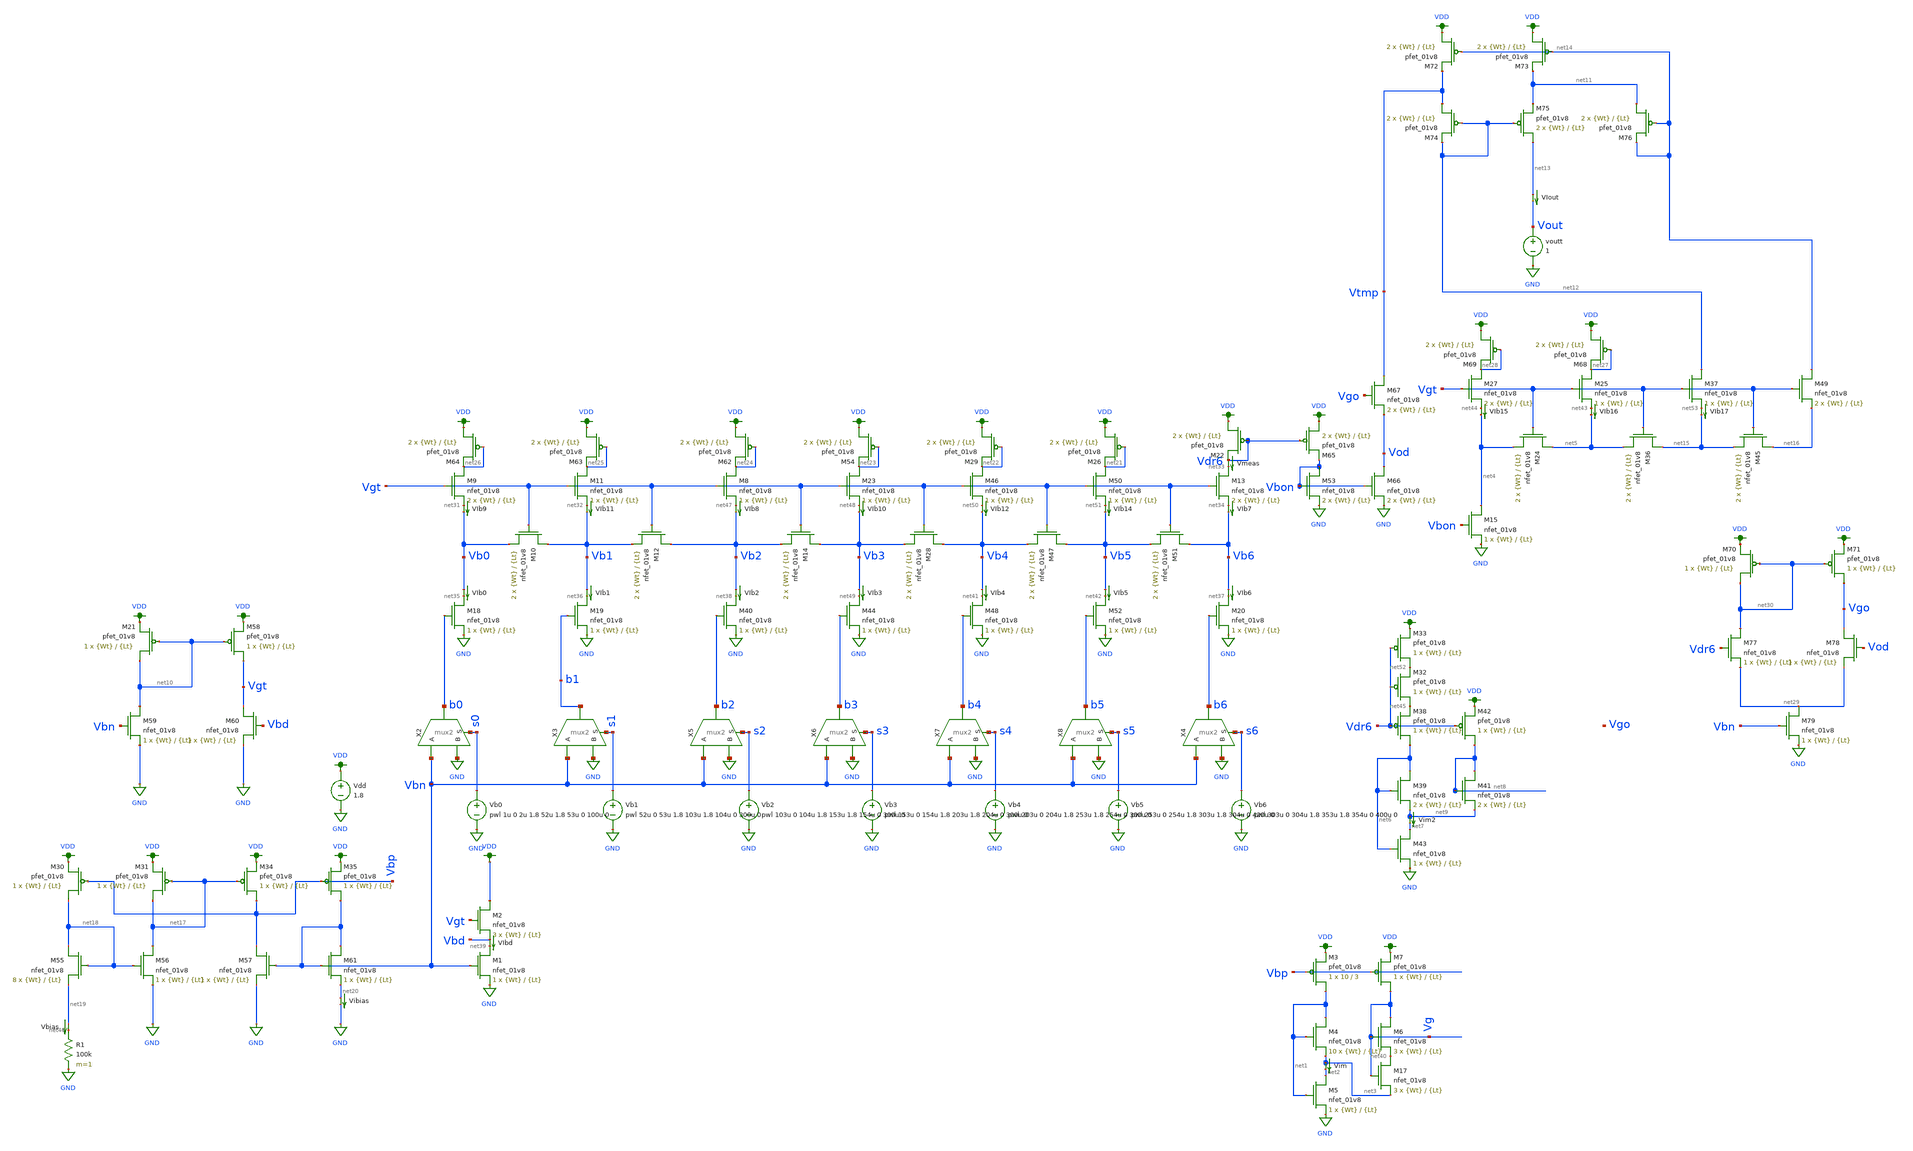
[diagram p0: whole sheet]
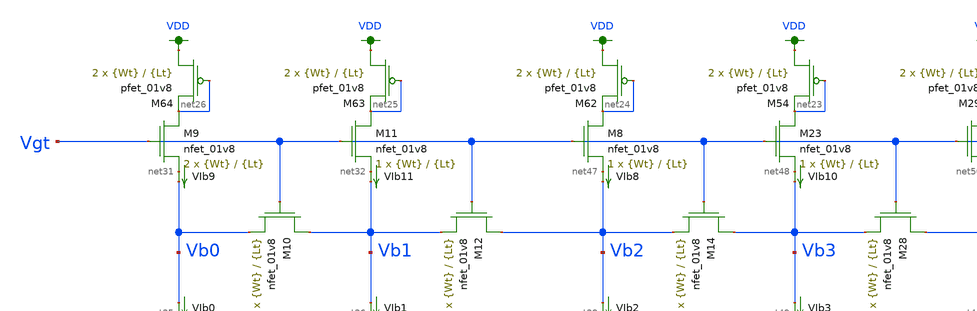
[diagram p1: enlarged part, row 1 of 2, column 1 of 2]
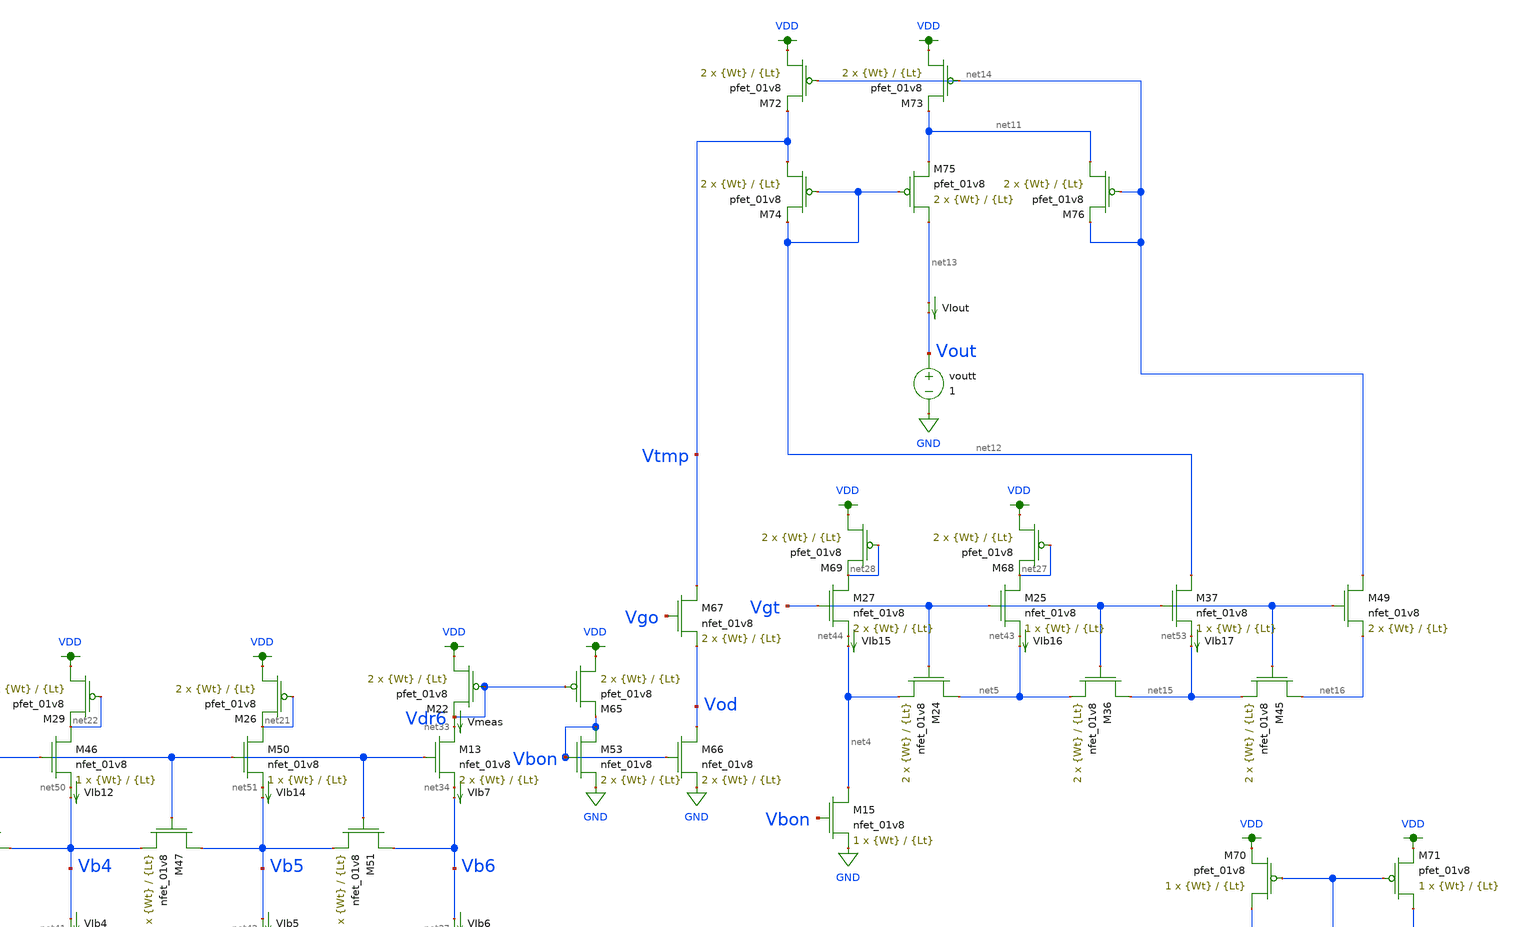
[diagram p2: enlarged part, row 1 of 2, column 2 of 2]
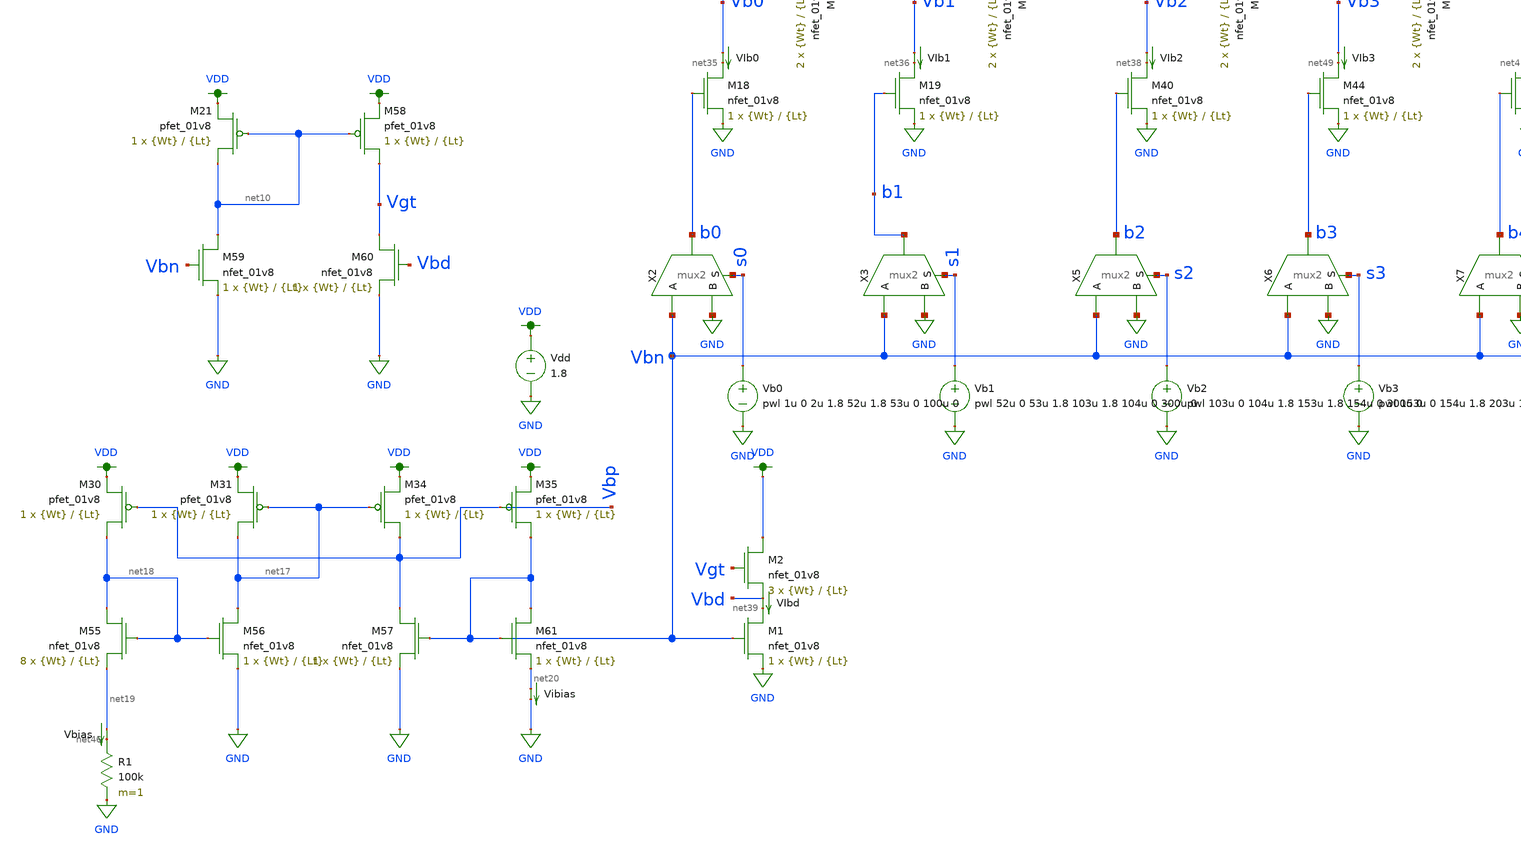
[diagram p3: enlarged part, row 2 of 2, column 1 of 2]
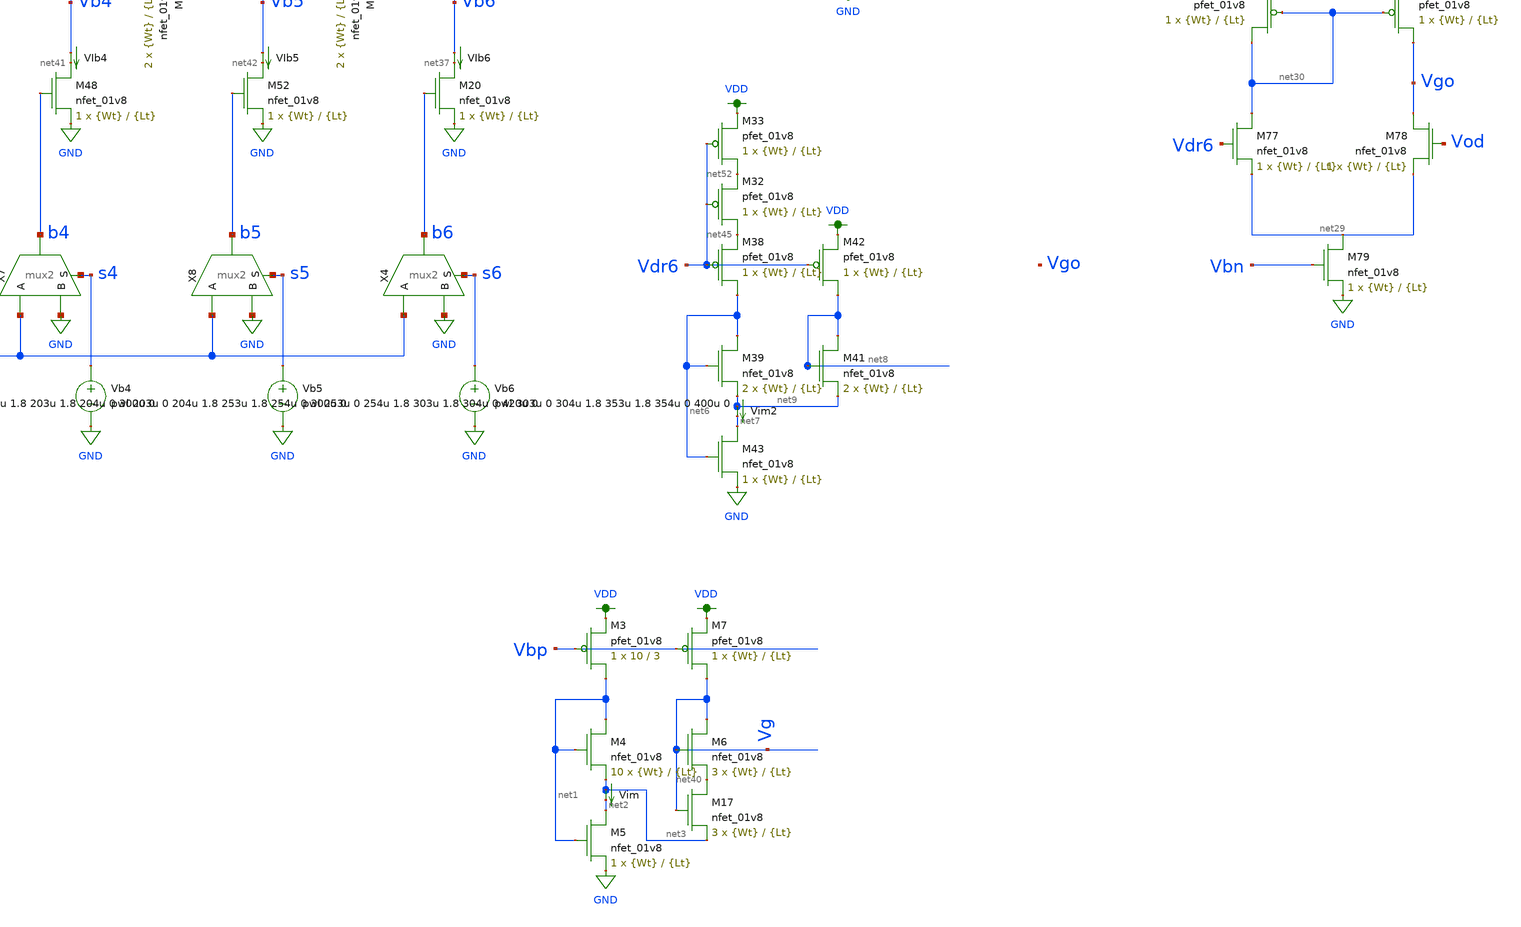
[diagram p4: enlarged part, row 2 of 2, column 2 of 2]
** sch_path: schematic/archive/dac7_test_josh_mywilson_idnl.sch
**.subckt dac7_test_josh_mywilson_idnl
X2 b0 Vbn GND s0 mux2
X3 b1 Vbn GND s1 mux2
Vdd VDD GND 1.8
Vb0 s0 GND pwl 1u 0 2u 1.8 52u 1.8 53u 0 100u 0
Vb1 s1 GND pwl 52u 0 53u 1.8 103u 1.8 104u 0 300u 0
Vb2 s2 GND pwl 103u 0 104u 1.8 153u 1.8 154u 0 300u 0
XM9 net26 Vgt net31 GND sky130_fd_pr__nfet_01v8 L={Lt} W={Wt} nf=1 ad='int((nf+1)/2) * W/nf * 0.29' as='int((nf+2)/2) * W/nf * 0.29'
+ pd='2*int((nf+1)/2) * (W/nf + 0.29)' ps='2*int((nf+2)/2) * (W/nf + 0.29)' nrd='0.29 / W' nrs='0.29 / W'
+ sa=0 sb=0 sd=0 mult=2 m=2
XM10 Vb1 Vgt Vb0 GND sky130_fd_pr__nfet_01v8 L={Lt} W={Wt} nf=1 ad='int((nf+1)/2) * W/nf * 0.29' as='int((nf+2)/2) * W/nf * 0.29'
+ pd='2*int((nf+1)/2) * (W/nf + 0.29)' ps='2*int((nf+2)/2) * (W/nf + 0.29)' nrd='0.29 / W' nrs='0.29 / W'
+ sa=0 sb=0 sd=0 mult=2 m=2
XM11 net25 Vgt net32 GND sky130_fd_pr__nfet_01v8 L={Lt} W={Wt} nf=1 ad='int((nf+1)/2) * W/nf * 0.29'
+ as='int((nf+2)/2) * W/nf * 0.29' pd='2*int((nf+1)/2) * (W/nf + 0.29)' ps='2*int((nf+2)/2) * (W/nf + 0.29)'
+ nrd='0.29 / W' nrs='0.29 / W' sa=0 sb=0 sd=0 mult=1 m=1
XM12 Vb2 Vgt Vb1 GND sky130_fd_pr__nfet_01v8 L={Lt} W={Wt} nf=1 ad='int((nf+1)/2) * W/nf * 0.29' as='int((nf+2)/2) * W/nf * 0.29'
+ pd='2*int((nf+1)/2) * (W/nf + 0.29)' ps='2*int((nf+2)/2) * (W/nf + 0.29)' nrd='0.29 / W' nrs='0.29 / W'
+ sa=0 sb=0 sd=0 mult=2 m=2
XM13 net33 Vgt net34 GND sky130_fd_pr__nfet_01v8 L={Lt} W={Wt} nf=1 ad='int((nf+1)/2) * W/nf * 0.29'
+ as='int((nf+2)/2) * W/nf * 0.29' pd='2*int((nf+1)/2) * (W/nf + 0.29)' ps='2*int((nf+2)/2) * (W/nf + 0.29)'
+ nrd='0.29 / W' nrs='0.29 / W' sa=0 sb=0 sd=0 mult=2 m=2
XM18 net35 b0 GND GND sky130_fd_pr__nfet_01v8 L={Lt} W={Wt} nf=1 ad='int((nf+1)/2) * W/nf * 0.29' as='int((nf+2)/2) * W/nf * 0.29'
+ pd='2*int((nf+1)/2) * (W/nf + 0.29)' ps='2*int((nf+2)/2) * (W/nf + 0.29)' nrd='0.29 / W' nrs='0.29 / W'
+ sa=0 sb=0 sd=0 mult=1 m=1
XM19 net36 b1 GND GND sky130_fd_pr__nfet_01v8 L={Lt} W={Wt} nf=1 ad='int((nf+1)/2) * W/nf * 0.29' as='int((nf+2)/2) * W/nf * 0.29'
+ pd='2*int((nf+1)/2) * (W/nf + 0.29)' ps='2*int((nf+2)/2) * (W/nf + 0.29)' nrd='0.29 / W' nrs='0.29 / W'
+ sa=0 sb=0 sd=0 mult=1 m=1
XM20 net37 b6 GND GND sky130_fd_pr__nfet_01v8 L={Lt} W={Wt} nf=1 ad='int((nf+1)/2) * W/nf * 0.29' as='int((nf+2)/2) * W/nf * 0.29'
+ pd='2*int((nf+1)/2) * (W/nf + 0.29)' ps='2*int((nf+2)/2) * (W/nf + 0.29)' nrd='0.29 / W' nrs='0.29 / W'
+ sa=0 sb=0 sd=0 mult=1 m=1
Vmeas Vdr6 net33 0
.save i(vmeas)
VIb0 Vb0 net35 0
.save i(vib0)
VIb1 Vb1 net36 0
.save i(vib1)
VIb2 Vb2 net38 0
.save i(vib2)
XM1 net39 Vbn GND GND sky130_fd_pr__nfet_01v8 L={Lt} W={Wt} nf=1 ad='int((nf+1)/2) * W/nf * 0.29' as='int((nf+2)/2) * W/nf * 0.29'
+ pd='2*int((nf+1)/2) * (W/nf + 0.29)' ps='2*int((nf+2)/2) * (W/nf + 0.29)' nrd='0.29 / W' nrs='0.29 / W'
+ sa=0 sb=0 sd=0 mult=1 m=1
VIbd Vbd net39 0
.save i(vibd)
XM3 net1 Vbp VDD VDD sky130_fd_pr__pfet_01v8 L=3 W=10 nf=1 ad='int((nf+1)/2) * W/nf * 0.29' as='int((nf+2)/2) * W/nf * 0.29'
+ pd='2*int((nf+1)/2) * (W/nf + 0.29)' ps='2*int((nf+2)/2) * (W/nf + 0.29)' nrd='0.29 / W' nrs='0.29 / W'
+ sa=0 sb=0 sd=0 mult=1 m=1
XM4 net1 net1 net3 GND sky130_fd_pr__nfet_01v8 L={Lt} W={Wt} nf=1 ad='int((nf+1)/2) * W/nf * 0.29' as='int((nf+2)/2) * W/nf * 0.29'
+ pd='2*int((nf+1)/2) * (W/nf + 0.29)' ps='2*int((nf+2)/2) * (W/nf + 0.29)' nrd='0.29 / W' nrs='0.29 / W'
+ sa=0 sb=0 sd=0 mult=10 m=10
XM5 net2 net1 GND GND sky130_fd_pr__nfet_01v8 L={Lt} W={Wt} nf=1 ad='int((nf+1)/2) * W/nf * 0.29' as='int((nf+2)/2) * W/nf * 0.29'
+ pd='2*int((nf+1)/2) * (W/nf + 0.29)' ps='2*int((nf+2)/2) * (W/nf + 0.29)' nrd='0.29 / W' nrs='0.29 / W'
+ sa=0 sb=0 sd=0 mult=1 m=1
Vim net3 net2 0
.save i(vim)
XM6 Vg Vg net40 GND sky130_fd_pr__nfet_01v8 L={Lt} W={Wt} nf=1 ad='int((nf+1)/2) * W/nf * 0.29' as='int((nf+2)/2) * W/nf * 0.29'
+ pd='2*int((nf+1)/2) * (W/nf + 0.29)' ps='2*int((nf+2)/2) * (W/nf + 0.29)' nrd='0.29 / W' nrs='0.29 / W'
+ sa=0 sb=0 sd=0 mult=3 m=3
XM7 Vg Vbp VDD VDD sky130_fd_pr__pfet_01v8 L={Lt} W={Wt} nf=1 ad='int((nf+1)/2) * W/nf * 0.29' as='int((nf+2)/2) * W/nf * 0.29'
+ pd='2*int((nf+1)/2) * (W/nf + 0.29)' ps='2*int((nf+2)/2) * (W/nf + 0.29)' nrd='0.29 / W' nrs='0.29 / W'
+ sa=0 sb=0 sd=0 mult=1 m=1
VIb4 Vb4 net41 0
.save i(vib4)
VIb5 Vb5 net42 0
.save i(vib5)
VIb6 Vb6 net37 0
.save i(vib6)
VIout net13 Vout 0
.save i(viout)
XM24 net5 Vgt net4 GND sky130_fd_pr__nfet_01v8 L={Lt} W={Wt} nf=1 ad='int((nf+1)/2) * W/nf * 0.29' as='int((nf+2)/2) * W/nf * 0.29'
+ pd='2*int((nf+1)/2) * (W/nf + 0.29)' ps='2*int((nf+2)/2) * (W/nf + 0.29)' nrd='0.29 / W' nrs='0.29 / W'
+ sa=0 sb=0 sd=0 mult=2 m=2
XM25 net27 Vgt net43 GND sky130_fd_pr__nfet_01v8 L={Lt} W={Wt} nf=1 ad='int((nf+1)/2) * W/nf * 0.29'
+ as='int((nf+2)/2) * W/nf * 0.29' pd='2*int((nf+1)/2) * (W/nf + 0.29)' ps='2*int((nf+2)/2) * (W/nf + 0.29)'
+ nrd='0.29 / W' nrs='0.29 / W' sa=0 sb=0 sd=0 mult=1 m=1
XM27 net28 Vgt net44 GND sky130_fd_pr__nfet_01v8 L={Lt} W={Wt} nf=1 ad='int((nf+1)/2) * W/nf * 0.29'
+ as='int((nf+2)/2) * W/nf * 0.29' pd='2*int((nf+1)/2) * (W/nf + 0.29)' ps='2*int((nf+2)/2) * (W/nf + 0.29)'
+ nrd='0.29 / W' nrs='0.29 / W' sa=0 sb=0 sd=0 mult=2 m=2
XM38 net6 Vdr6 net45 VDD sky130_fd_pr__pfet_01v8 L={Lt} W={Wt} nf=1 ad='int((nf+1)/2) * W/nf * 0.29'
+ as='int((nf+2)/2) * W/nf * 0.29' pd='2*int((nf+1)/2) * (W/nf + 0.29)' ps='2*int((nf+2)/2) * (W/nf + 0.29)'
+ nrd='0.29 / W' nrs='0.29 / W' sa=0 sb=0 sd=0 mult=1 m=1
XM39 net6 net6 net9 GND sky130_fd_pr__nfet_01v8 L={Lt} W={Wt} nf=1 ad='int((nf+1)/2) * W/nf * 0.29' as='int((nf+2)/2) * W/nf * 0.29'
+ pd='2*int((nf+1)/2) * (W/nf + 0.29)' ps='2*int((nf+2)/2) * (W/nf + 0.29)' nrd='0.29 / W' nrs='0.29 / W'
+ sa=0 sb=0 sd=0 mult=2 m=2
Vim2 net9 net7 0
.save i(vim2)
XM41 net8 net8 net9 GND sky130_fd_pr__nfet_01v8 L={Lt} W={Wt} nf=1 ad='int((nf+1)/2) * W/nf * 0.29' as='int((nf+2)/2) * W/nf * 0.29'
+ pd='2*int((nf+1)/2) * (W/nf + 0.29)' ps='2*int((nf+2)/2) * (W/nf + 0.29)' nrd='0.29 / W' nrs='0.29 / W'
+ sa=0 sb=0 sd=0 mult=2 m=2
XM42 net8 Vdr6 VDD VDD sky130_fd_pr__pfet_01v8 L={Lt} W={Wt} nf=1 ad='int((nf+1)/2) * W/nf * 0.29' as='int((nf+2)/2) * W/nf * 0.29'
+ pd='2*int((nf+1)/2) * (W/nf + 0.29)' ps='2*int((nf+2)/2) * (W/nf + 0.29)' nrd='0.29 / W' nrs='0.29 / W'
+ sa=0 sb=0 sd=0 mult=1 m=1
XM43 net7 net6 GND GND sky130_fd_pr__nfet_01v8 L={Lt} W={Wt} nf=1 ad='int((nf+1)/2) * W/nf * 0.29' as='int((nf+2)/2) * W/nf * 0.29'
+ pd='2*int((nf+1)/2) * (W/nf + 0.29)' ps='2*int((nf+2)/2) * (W/nf + 0.29)' nrd='0.29 / W' nrs='0.29 / W'
+ sa=0 sb=0 sd=0 mult=1 m=1
XM2 VDD Vgt Vbd GND sky130_fd_pr__nfet_01v8 L={Lt} W={Wt} nf=1 ad='int((nf+1)/2) * W/nf * 0.29' as='int((nf+2)/2) * W/nf * 0.29'
+ pd='2*int((nf+1)/2) * (W/nf + 0.29)' ps='2*int((nf+2)/2) * (W/nf + 0.29)' nrd='0.29 / W' nrs='0.29 / W'
+ sa=0 sb=0 sd=0 mult=3 m=3
XM17 net40 Vg net3 GND sky130_fd_pr__nfet_01v8 L={Lt} W={Wt} nf=1 ad='int((nf+1)/2) * W/nf * 0.29' as='int((nf+2)/2) * W/nf * 0.29'
+ pd='2*int((nf+1)/2) * (W/nf + 0.29)' ps='2*int((nf+2)/2) * (W/nf + 0.29)' nrd='0.29 / W' nrs='0.29 / W'
+ sa=0 sb=0 sd=0 mult=3 m=3
XM21 net10 net10 VDD VDD sky130_fd_pr__pfet_01v8 L={Lt} W={Wt} nf=1 ad='int((nf+1)/2) * W/nf * 0.29'
+ as='int((nf+2)/2) * W/nf * 0.29' pd='2*int((nf+1)/2) * (W/nf + 0.29)' ps='2*int((nf+2)/2) * (W/nf + 0.29)'
+ nrd='0.29 / W' nrs='0.29 / W' sa=0 sb=0 sd=0 mult=1 m=1
XM58 Vgt net10 VDD VDD sky130_fd_pr__pfet_01v8 L={Lt} W={Wt} nf=1 ad='int((nf+1)/2) * W/nf * 0.29' as='int((nf+2)/2) * W/nf * 0.29'
+ pd='2*int((nf+1)/2) * (W/nf + 0.29)' ps='2*int((nf+2)/2) * (W/nf + 0.29)' nrd='0.29 / W' nrs='0.29 / W'
+ sa=0 sb=0 sd=0 mult=1 m=1
XM59 net10 Vbn GND GND sky130_fd_pr__nfet_01v8 L={Lt} W={Wt} nf=1 ad='int((nf+1)/2) * W/nf * 0.29' as='int((nf+2)/2) * W/nf * 0.29'
+ pd='2*int((nf+1)/2) * (W/nf + 0.29)' ps='2*int((nf+2)/2) * (W/nf + 0.29)' nrd='0.29 / W' nrs='0.29 / W'
+ sa=0 sb=0 sd=0 mult=1 m=1
XM60 Vgt Vbd GND GND sky130_fd_pr__nfet_01v8 L={Lt} W={Wt} nf=1 ad='int((nf+1)/2) * W/nf * 0.29' as='int((nf+2)/2) * W/nf * 0.29'
+ pd='2*int((nf+1)/2) * (W/nf + 0.29)' ps='2*int((nf+2)/2) * (W/nf + 0.29)' nrd='0.29 / W' nrs='0.29 / W'
+ sa=0 sb=0 sd=0 mult=1 m=1
XM72 VDD net14 Vtmp VDD sky130_fd_pr__pfet_01v8 L={Lt} W={Wt} nf=1 ad='int((nf+1)/2) * W/nf * 0.29' as='int((nf+2)/2) * W/nf * 0.29'
+ pd='2*int((nf+1)/2) * (W/nf + 0.29)' ps='2*int((nf+2)/2) * (W/nf + 0.29)' nrd='0.29 / W' nrs='0.29 / W'
+ sa=0 sb=0 sd=0 mult=2 m=2
XM73 VDD net14 net11 VDD sky130_fd_pr__pfet_01v8 L={Lt} W={Wt} nf=1 ad='int((nf+1)/2) * W/nf * 0.29'
+ as='int((nf+2)/2) * W/nf * 0.29' pd='2*int((nf+1)/2) * (W/nf + 0.29)' ps='2*int((nf+2)/2) * (W/nf + 0.29)'
+ nrd='0.29 / W' nrs='0.29 / W' sa=0 sb=0 sd=0 mult=2 m=2
XM74 Vtmp net12 net12 VDD sky130_fd_pr__pfet_01v8 L={Lt} W={Wt} nf=1 ad='int((nf+1)/2) * W/nf * 0.29'
+ as='int((nf+2)/2) * W/nf * 0.29' pd='2*int((nf+1)/2) * (W/nf + 0.29)' ps='2*int((nf+2)/2) * (W/nf + 0.29)'
+ nrd='0.29 / W' nrs='0.29 / W' sa=0 sb=0 sd=0 mult=2 m=2
XM75 net13 net12 net11 VDD sky130_fd_pr__pfet_01v8 L={Lt} W={Wt} nf=1 ad='int((nf+1)/2) * W/nf * 0.29'
+ as='int((nf+2)/2) * W/nf * 0.29' pd='2*int((nf+1)/2) * (W/nf + 0.29)' ps='2*int((nf+2)/2) * (W/nf + 0.29)'
+ nrd='0.29 / W' nrs='0.29 / W' sa=0 sb=0 sd=0 mult=2 m=2
XM76 net11 net14 net14 VDD sky130_fd_pr__pfet_01v8 L={Lt} W={Wt} nf=1 ad='int((nf+1)/2) * W/nf * 0.29'
+ as='int((nf+2)/2) * W/nf * 0.29' pd='2*int((nf+1)/2) * (W/nf + 0.29)' ps='2*int((nf+2)/2) * (W/nf + 0.29)'
+ nrd='0.29 / W' nrs='0.29 / W' sa=0 sb=0 sd=0 mult=2 m=2
R1 net46 GND 100k m=1
Vbias net19 net46 0
.save i(vbias)
X5 b2 Vbn GND s2 mux2
Vb3 s3 GND pwl 153u 0 154u 1.8 203u 1.8 204u 0 300u 0
XM8 net24 Vgt net47 GND sky130_fd_pr__nfet_01v8 L={Lt} W={Wt} nf=1 ad='int((nf+1)/2) * W/nf * 0.29' as='int((nf+2)/2) * W/nf * 0.29'
+ pd='2*int((nf+1)/2) * (W/nf + 0.29)' ps='2*int((nf+2)/2) * (W/nf + 0.29)' nrd='0.29 / W' nrs='0.29 / W'
+ sa=0 sb=0 sd=0 mult=1 m=1
XM14 Vb3 Vgt Vb2 GND sky130_fd_pr__nfet_01v8 L={Lt} W={Wt} nf=1 ad='int((nf+1)/2) * W/nf * 0.29' as='int((nf+2)/2) * W/nf * 0.29'
+ pd='2*int((nf+1)/2) * (W/nf + 0.29)' ps='2*int((nf+2)/2) * (W/nf + 0.29)' nrd='0.29 / W' nrs='0.29 / W'
+ sa=0 sb=0 sd=0 mult=2 m=2
XM40 net38 b2 GND GND sky130_fd_pr__nfet_01v8 L={Lt} W={Wt} nf=1 ad='int((nf+1)/2) * W/nf * 0.29' as='int((nf+2)/2) * W/nf * 0.29'
+ pd='2*int((nf+1)/2) * (W/nf + 0.29)' ps='2*int((nf+2)/2) * (W/nf + 0.29)' nrd='0.29 / W' nrs='0.29 / W'
+ sa=0 sb=0 sd=0 mult=1 m=1
VIb7 net34 Vb6 0
.save i(vib7)
VIb8 net47 Vb2 0
.save i(vib8)
X6 b3 Vbn GND s3 mux2
Vb4 s4 GND pwl 203u 0 204u 1.8 253u 1.8 254u 0 300u 0
XM23 net23 Vgt net48 GND sky130_fd_pr__nfet_01v8 L={Lt} W={Wt} nf=1 ad='int((nf+1)/2) * W/nf * 0.29'
+ as='int((nf+2)/2) * W/nf * 0.29' pd='2*int((nf+1)/2) * (W/nf + 0.29)' ps='2*int((nf+2)/2) * (W/nf + 0.29)'
+ nrd='0.29 / W' nrs='0.29 / W' sa=0 sb=0 sd=0 mult=1 m=1
XM28 Vb4 Vgt Vb3 GND sky130_fd_pr__nfet_01v8 L={Lt} W={Wt} nf=1 ad='int((nf+1)/2) * W/nf * 0.29' as='int((nf+2)/2) * W/nf * 0.29'
+ pd='2*int((nf+1)/2) * (W/nf + 0.29)' ps='2*int((nf+2)/2) * (W/nf + 0.29)' nrd='0.29 / W' nrs='0.29 / W'
+ sa=0 sb=0 sd=0 mult=2 m=2
XM44 net49 b3 GND GND sky130_fd_pr__nfet_01v8 L={Lt} W={Wt} nf=1 ad='int((nf+1)/2) * W/nf * 0.29' as='int((nf+2)/2) * W/nf * 0.29'
+ pd='2*int((nf+1)/2) * (W/nf + 0.29)' ps='2*int((nf+2)/2) * (W/nf + 0.29)' nrd='0.29 / W' nrs='0.29 / W'
+ sa=0 sb=0 sd=0 mult=1 m=1
VIb3 Vb3 net49 0
.save i(vib3)
VIb10 net48 Vb3 0
.save i(vib10)
X7 b4 Vbn GND s4 mux2
Vb5 s5 GND pwl 253u 0 254u 1.8 303u 1.8 304u 0 420u 0
XM46 net22 Vgt net50 GND sky130_fd_pr__nfet_01v8 L={Lt} W={Wt} nf=1 ad='int((nf+1)/2) * W/nf * 0.29'
+ as='int((nf+2)/2) * W/nf * 0.29' pd='2*int((nf+1)/2) * (W/nf + 0.29)' ps='2*int((nf+2)/2) * (W/nf + 0.29)'
+ nrd='0.29 / W' nrs='0.29 / W' sa=0 sb=0 sd=0 mult=1 m=1
XM47 Vb5 Vgt Vb4 GND sky130_fd_pr__nfet_01v8 L={Lt} W={Wt} nf=1 ad='int((nf+1)/2) * W/nf * 0.29' as='int((nf+2)/2) * W/nf * 0.29'
+ pd='2*int((nf+1)/2) * (W/nf + 0.29)' ps='2*int((nf+2)/2) * (W/nf + 0.29)' nrd='0.29 / W' nrs='0.29 / W'
+ sa=0 sb=0 sd=0 mult=2 m=2
XM48 net41 b4 GND GND sky130_fd_pr__nfet_01v8 L={Lt} W={Wt} nf=1 ad='int((nf+1)/2) * W/nf * 0.29' as='int((nf+2)/2) * W/nf * 0.29'
+ pd='2*int((nf+1)/2) * (W/nf + 0.29)' ps='2*int((nf+2)/2) * (W/nf + 0.29)' nrd='0.29 / W' nrs='0.29 / W'
+ sa=0 sb=0 sd=0 mult=1 m=1
VIb9 net31 Vb0 0
.save i(vib9)
VIb12 net50 Vb4 0
.save i(vib12)
X8 b5 Vbn GND s5 mux2
XM50 net21 Vgt net51 GND sky130_fd_pr__nfet_01v8 L={Lt} W={Wt} nf=1 ad='int((nf+1)/2) * W/nf * 0.29'
+ as='int((nf+2)/2) * W/nf * 0.29' pd='2*int((nf+1)/2) * (W/nf + 0.29)' ps='2*int((nf+2)/2) * (W/nf + 0.29)'
+ nrd='0.29 / W' nrs='0.29 / W' sa=0 sb=0 sd=0 mult=1 m=1
XM51 Vb6 Vgt Vb5 GND sky130_fd_pr__nfet_01v8 L={Lt} W={Wt} nf=1 ad='int((nf+1)/2) * W/nf * 0.29' as='int((nf+2)/2) * W/nf * 0.29'
+ pd='2*int((nf+1)/2) * (W/nf + 0.29)' ps='2*int((nf+2)/2) * (W/nf + 0.29)' nrd='0.29 / W' nrs='0.29 / W'
+ sa=0 sb=0 sd=0 mult=2 m=2
XM52 net42 b5 GND GND sky130_fd_pr__nfet_01v8 L={Lt} W={Wt} nf=1 ad='int((nf+1)/2) * W/nf * 0.29' as='int((nf+2)/2) * W/nf * 0.29'
+ pd='2*int((nf+1)/2) * (W/nf + 0.29)' ps='2*int((nf+2)/2) * (W/nf + 0.29)' nrd='0.29 / W' nrs='0.29 / W'
+ sa=0 sb=0 sd=0 mult=1 m=1
VIb11 net32 Vb1 0
.save i(vib11)
VIb14 net51 Vb5 0
.save i(vib14)
Vb6 s6 GND pwl 303u 0 304u 1.8 353u 1.8 354u 0 400u 0
X4 b6 Vbn GND s6 mux2
XM32 net45 Vdr6 net52 VDD sky130_fd_pr__pfet_01v8 L={Lt} W={Wt} nf=1 ad='int((nf+1)/2) * W/nf * 0.29'
+ as='int((nf+2)/2) * W/nf * 0.29' pd='2*int((nf+1)/2) * (W/nf + 0.29)' ps='2*int((nf+2)/2) * (W/nf + 0.29)'
+ nrd='0.29 / W' nrs='0.29 / W' sa=0 sb=0 sd=0 mult=1 m=1
XM33 net52 Vdr6 VDD VDD sky130_fd_pr__pfet_01v8 L={Lt} W={Wt} nf=1 ad='int((nf+1)/2) * W/nf * 0.29' as='int((nf+2)/2) * W/nf * 0.29'
+ pd='2*int((nf+1)/2) * (W/nf + 0.29)' ps='2*int((nf+2)/2) * (W/nf + 0.29)' nrd='0.29 / W' nrs='0.29 / W'
+ sa=0 sb=0 sd=0 mult=1 m=1
XM15 net4 Vbon GND GND sky130_fd_pr__nfet_01v8 L={Lt} W={Wt} nf=1 ad='int((nf+1)/2) * W/nf * 0.29' as='int((nf+2)/2) * W/nf * 0.29'
+ pd='2*int((nf+1)/2) * (W/nf + 0.29)' ps='2*int((nf+2)/2) * (W/nf + 0.29)' nrd='0.29 / W' nrs='0.29 / W'
+ sa=0 sb=0 sd=0 mult=1 m=1
XM36 net15 Vgt net5 GND sky130_fd_pr__nfet_01v8 L={Lt} W={Wt} nf=1 ad='int((nf+1)/2) * W/nf * 0.29' as='int((nf+2)/2) * W/nf * 0.29'
+ pd='2*int((nf+1)/2) * (W/nf + 0.29)' ps='2*int((nf+2)/2) * (W/nf + 0.29)' nrd='0.29 / W' nrs='0.29 / W'
+ sa=0 sb=0 sd=0 mult=2 m=2
XM37 net12 Vgt net53 GND sky130_fd_pr__nfet_01v8 L={Lt} W={Wt} nf=1 ad='int((nf+1)/2) * W/nf * 0.29'
+ as='int((nf+2)/2) * W/nf * 0.29' pd='2*int((nf+1)/2) * (W/nf + 0.29)' ps='2*int((nf+2)/2) * (W/nf + 0.29)'
+ nrd='0.29 / W' nrs='0.29 / W' sa=0 sb=0 sd=0 mult=1 m=1
VIb15 net44 net4 0
.save i(vib15)
VIb16 net43 net5 0
.save i(vib16)
VIb17 net53 net15 0
.save i(vib17)
XM45 net16 Vgt net15 GND sky130_fd_pr__nfet_01v8 L={Lt} W={Wt} nf=1 ad='int((nf+1)/2) * W/nf * 0.29'
+ as='int((nf+2)/2) * W/nf * 0.29' pd='2*int((nf+1)/2) * (W/nf + 0.29)' ps='2*int((nf+2)/2) * (W/nf + 0.29)'
+ nrd='0.29 / W' nrs='0.29 / W' sa=0 sb=0 sd=0 mult=2 m=2
XM49 net14 Vgt net16 GND sky130_fd_pr__nfet_01v8 L={Lt} W={Wt} nf=1 ad='int((nf+1)/2) * W/nf * 0.29'
+ as='int((nf+2)/2) * W/nf * 0.29' pd='2*int((nf+1)/2) * (W/nf + 0.29)' ps='2*int((nf+2)/2) * (W/nf + 0.29)'
+ nrd='0.29 / W' nrs='0.29 / W' sa=0 sb=0 sd=0 mult=2 m=2
XM30 net18 Vbp VDD VDD sky130_fd_pr__pfet_01v8 L={Lt} W={Wt} nf=1 ad='int((nf+1)/2) * W/nf * 0.29' as='int((nf+2)/2) * W/nf * 0.29'
+ pd='2*int((nf+1)/2) * (W/nf + 0.29)' ps='2*int((nf+2)/2) * (W/nf + 0.29)' nrd='0.29 / W' nrs='0.29 / W'
+ sa=0 sb=0 sd=0 mult=1 m=1
XM31 net17 net17 VDD VDD sky130_fd_pr__pfet_01v8 L={Lt} W={Wt} nf=1 ad='int((nf+1)/2) * W/nf * 0.29'
+ as='int((nf+2)/2) * W/nf * 0.29' pd='2*int((nf+1)/2) * (W/nf + 0.29)' ps='2*int((nf+2)/2) * (W/nf + 0.29)'
+ nrd='0.29 / W' nrs='0.29 / W' sa=0 sb=0 sd=0 mult=1 m=1
XM34 Vbp net17 VDD VDD sky130_fd_pr__pfet_01v8 L={Lt} W={Wt} nf=1 ad='int((nf+1)/2) * W/nf * 0.29' as='int((nf+2)/2) * W/nf * 0.29'
+ pd='2*int((nf+1)/2) * (W/nf + 0.29)' ps='2*int((nf+2)/2) * (W/nf + 0.29)' nrd='0.29 / W' nrs='0.29 / W'
+ sa=0 sb=0 sd=0 mult=1 m=1
XM35 Vbn Vbp VDD VDD sky130_fd_pr__pfet_01v8 L={Lt} W={Wt} nf=1 ad='int((nf+1)/2) * W/nf * 0.29' as='int((nf+2)/2) * W/nf * 0.29'
+ pd='2*int((nf+1)/2) * (W/nf + 0.29)' ps='2*int((nf+2)/2) * (W/nf + 0.29)' nrd='0.29 / W' nrs='0.29 / W'
+ sa=0 sb=0 sd=0 mult=1 m=1
XM55 net18 net18 net19 GND sky130_fd_pr__nfet_01v8 L={Lt} W={Wt} nf=1 ad='int((nf+1)/2) * W/nf * 0.29'
+ as='int((nf+2)/2) * W/nf * 0.29' pd='2*int((nf+1)/2) * (W/nf + 0.29)' ps='2*int((nf+2)/2) * (W/nf + 0.29)'
+ nrd='0.29 / W' nrs='0.29 / W' sa=0 sb=0 sd=0 mult=8 m=8
XM56 net17 net18 GND GND sky130_fd_pr__nfet_01v8 L={Lt} W={Wt} nf=1 ad='int((nf+1)/2) * W/nf * 0.29'
+ as='int((nf+2)/2) * W/nf * 0.29' pd='2*int((nf+1)/2) * (W/nf + 0.29)' ps='2*int((nf+2)/2) * (W/nf + 0.29)'
+ nrd='0.29 / W' nrs='0.29 / W' sa=0 sb=0 sd=0 mult=1 m=1
XM57 Vbp Vbn GND GND sky130_fd_pr__nfet_01v8 L={Lt} W={Wt} nf=1 ad='int((nf+1)/2) * W/nf * 0.29' as='int((nf+2)/2) * W/nf * 0.29'
+ pd='2*int((nf+1)/2) * (W/nf + 0.29)' ps='2*int((nf+2)/2) * (W/nf + 0.29)' nrd='0.29 / W' nrs='0.29 / W'
+ sa=0 sb=0 sd=0 mult=1 m=1
XM61 Vbn Vbn net20 GND sky130_fd_pr__nfet_01v8 L={Lt} W={Wt} nf=1 ad='int((nf+1)/2) * W/nf * 0.29' as='int((nf+2)/2) * W/nf * 0.29'
+ pd='2*int((nf+1)/2) * (W/nf + 0.29)' ps='2*int((nf+2)/2) * (W/nf + 0.29)' nrd='0.29 / W' nrs='0.29 / W'
+ sa=0 sb=0 sd=0 mult=1 m=1
Vibias net20 GND 0
.save i(vibias)
XM53 Vbon Vbon GND GND sky130_fd_pr__nfet_01v8 L={Lt} W={Wt} nf=1 ad='int((nf+1)/2) * W/nf * 0.29' as='int((nf+2)/2) * W/nf * 0.29'
+ pd='2*int((nf+1)/2) * (W/nf + 0.29)' ps='2*int((nf+2)/2) * (W/nf + 0.29)' nrd='0.29 / W' nrs='0.29 / W'
+ sa=0 sb=0 sd=0 mult=2 m=2
XM22 VDD Vdr6 Vdr6 VDD sky130_fd_pr__pfet_01v8 L={Lt} W={Wt} nf=1 ad='int((nf+1)/2) * W/nf * 0.29' as='int((nf+2)/2) * W/nf * 0.29'
+ pd='2*int((nf+1)/2) * (W/nf + 0.29)' ps='2*int((nf+2)/2) * (W/nf + 0.29)' nrd='0.29 / W' nrs='0.29 / W'
+ sa=0 sb=0 sd=0 mult=2 m=2
XM26 VDD net21 net21 VDD sky130_fd_pr__pfet_01v8 L={Lt} W={Wt} nf=1 ad='int((nf+1)/2) * W/nf * 0.29'
+ as='int((nf+2)/2) * W/nf * 0.29' pd='2*int((nf+1)/2) * (W/nf + 0.29)' ps='2*int((nf+2)/2) * (W/nf + 0.29)'
+ nrd='0.29 / W' nrs='0.29 / W' sa=0 sb=0 sd=0 mult=2 m=2
XM29 VDD net22 net22 VDD sky130_fd_pr__pfet_01v8 L={Lt} W={Wt} nf=1 ad='int((nf+1)/2) * W/nf * 0.29'
+ as='int((nf+2)/2) * W/nf * 0.29' pd='2*int((nf+1)/2) * (W/nf + 0.29)' ps='2*int((nf+2)/2) * (W/nf + 0.29)'
+ nrd='0.29 / W' nrs='0.29 / W' sa=0 sb=0 sd=0 mult=2 m=2
XM54 VDD net23 net23 VDD sky130_fd_pr__pfet_01v8 L={Lt} W={Wt} nf=1 ad='int((nf+1)/2) * W/nf * 0.29'
+ as='int((nf+2)/2) * W/nf * 0.29' pd='2*int((nf+1)/2) * (W/nf + 0.29)' ps='2*int((nf+2)/2) * (W/nf + 0.29)'
+ nrd='0.29 / W' nrs='0.29 / W' sa=0 sb=0 sd=0 mult=2 m=2
XM62 VDD net24 net24 VDD sky130_fd_pr__pfet_01v8 L={Lt} W={Wt} nf=1 ad='int((nf+1)/2) * W/nf * 0.29'
+ as='int((nf+2)/2) * W/nf * 0.29' pd='2*int((nf+1)/2) * (W/nf + 0.29)' ps='2*int((nf+2)/2) * (W/nf + 0.29)'
+ nrd='0.29 / W' nrs='0.29 / W' sa=0 sb=0 sd=0 mult=2 m=2
XM63 VDD net25 net25 VDD sky130_fd_pr__pfet_01v8 L={Lt} W={Wt} nf=1 ad='int((nf+1)/2) * W/nf * 0.29'
+ as='int((nf+2)/2) * W/nf * 0.29' pd='2*int((nf+1)/2) * (W/nf + 0.29)' ps='2*int((nf+2)/2) * (W/nf + 0.29)'
+ nrd='0.29 / W' nrs='0.29 / W' sa=0 sb=0 sd=0 mult=2 m=2
XM64 VDD net26 net26 VDD sky130_fd_pr__pfet_01v8 L={Lt} W={Wt} nf=1 ad='int((nf+1)/2) * W/nf * 0.29'
+ as='int((nf+2)/2) * W/nf * 0.29' pd='2*int((nf+1)/2) * (W/nf + 0.29)' ps='2*int((nf+2)/2) * (W/nf + 0.29)'
+ nrd='0.29 / W' nrs='0.29 / W' sa=0 sb=0 sd=0 mult=2 m=2
XM65 VDD Vdr6 Vbon VDD sky130_fd_pr__pfet_01v8 L={Lt} W={Wt} nf=1 ad='int((nf+1)/2) * W/nf * 0.29' as='int((nf+2)/2) * W/nf * 0.29'
+ pd='2*int((nf+1)/2) * (W/nf + 0.29)' ps='2*int((nf+2)/2) * (W/nf + 0.29)' nrd='0.29 / W' nrs='0.29 / W'
+ sa=0 sb=0 sd=0 mult=2 m=2
XM66 Vod Vbon GND GND sky130_fd_pr__nfet_01v8 L={Lt} W={Wt} nf=1 ad='int((nf+1)/2) * W/nf * 0.29' as='int((nf+2)/2) * W/nf * 0.29'
+ pd='2*int((nf+1)/2) * (W/nf + 0.29)' ps='2*int((nf+2)/2) * (W/nf + 0.29)' nrd='0.29 / W' nrs='0.29 / W'
+ sa=0 sb=0 sd=0 mult=2 m=2
XM68 VDD net27 net27 VDD sky130_fd_pr__pfet_01v8 L={Lt} W={Wt} nf=1 ad='int((nf+1)/2) * W/nf * 0.29'
+ as='int((nf+2)/2) * W/nf * 0.29' pd='2*int((nf+1)/2) * (W/nf + 0.29)' ps='2*int((nf+2)/2) * (W/nf + 0.29)'
+ nrd='0.29 / W' nrs='0.29 / W' sa=0 sb=0 sd=0 mult=2 m=2
XM69 VDD net28 net28 VDD sky130_fd_pr__pfet_01v8 L={Lt} W={Wt} nf=1 ad='int((nf+1)/2) * W/nf * 0.29'
+ as='int((nf+2)/2) * W/nf * 0.29' pd='2*int((nf+1)/2) * (W/nf + 0.29)' ps='2*int((nf+2)/2) * (W/nf + 0.29)'
+ nrd='0.29 / W' nrs='0.29 / W' sa=0 sb=0 sd=0 mult=2 m=2
XM70 net30 net30 VDD VDD sky130_fd_pr__pfet_01v8 L={Lt} W={Wt} nf=1 ad='int((nf+1)/2) * W/nf * 0.29'
+ as='int((nf+2)/2) * W/nf * 0.29' pd='2*int((nf+1)/2) * (W/nf + 0.29)' ps='2*int((nf+2)/2) * (W/nf + 0.29)'
+ nrd='0.29 / W' nrs='0.29 / W' sa=0 sb=0 sd=0 mult=1 m=1
XM71 Vgo net30 VDD VDD sky130_fd_pr__pfet_01v8 L={Lt} W={Wt} nf=1 ad='int((nf+1)/2) * W/nf * 0.29' as='int((nf+2)/2) * W/nf * 0.29'
+ pd='2*int((nf+1)/2) * (W/nf + 0.29)' ps='2*int((nf+2)/2) * (W/nf + 0.29)' nrd='0.29 / W' nrs='0.29 / W'
+ sa=0 sb=0 sd=0 mult=1 m=1
XM77 net30 Vdr6 net29 GND sky130_fd_pr__nfet_01v8 L={Lt} W={Wt} nf=1 ad='int((nf+1)/2) * W/nf * 0.29'
+ as='int((nf+2)/2) * W/nf * 0.29' pd='2*int((nf+1)/2) * (W/nf + 0.29)' ps='2*int((nf+2)/2) * (W/nf + 0.29)'
+ nrd='0.29 / W' nrs='0.29 / W' sa=0 sb=0 sd=0 mult=1 m=1
XM78 Vgo Vod net29 GND sky130_fd_pr__nfet_01v8 L={Lt} W={Wt} nf=1 ad='int((nf+1)/2) * W/nf * 0.29' as='int((nf+2)/2) * W/nf * 0.29'
+ pd='2*int((nf+1)/2) * (W/nf + 0.29)' ps='2*int((nf+2)/2) * (W/nf + 0.29)' nrd='0.29 / W' nrs='0.29 / W'
+ sa=0 sb=0 sd=0 mult=1 m=1
XM67 Vtmp Vgo Vod GND sky130_fd_pr__nfet_01v8 L={Lt} W={Wt} nf=1 ad='int((nf+1)/2) * W/nf * 0.29' as='int((nf+2)/2) * W/nf * 0.29'
+ pd='2*int((nf+1)/2) * (W/nf + 0.29)' ps='2*int((nf+2)/2) * (W/nf + 0.29)' nrd='0.29 / W' nrs='0.29 / W'
+ sa=0 sb=0 sd=0 mult=2 m=2
XM79 net29 Vbn GND GND sky130_fd_pr__nfet_01v8 L={Lt} W={Wt} nf=1 ad='int((nf+1)/2) * W/nf * 0.29' as='int((nf+2)/2) * W/nf * 0.29'
+ pd='2*int((nf+1)/2) * (W/nf + 0.29)' ps='2*int((nf+2)/2) * (W/nf + 0.29)' nrd='0.29 / W' nrs='0.29 / W'
+ sa=0 sb=0 sd=0 mult=1 m=1
voutt Vout GND 1
**** begin user architecture code

.option wnflag=1
.param MC_SWITCH=1.0
.lib ~/skywater/skywater-pdk/libraries/sky130_fd_pr_ngspice/latest/models/sky130.lib.spice tt


.param Wt = 16
.param Lt = 4
.control
*** change W and L for the next two lines as well !***
  let myW = 3
  let myL = 1
  set wr_singlescale
  let runs = 10
  let run = 1
  while run <= runs
    set appendwrite = FALSE
    set wr_vecnames
    let code = 0
    while code < 64
      if code eq 0
        let b0 = 0
      else
        let b0 = (code % 2) * 1.8
      end
      if floor(code / 2) eq 0
        let b1 = 0
      else
        let b1 = (floor(code / 2) % 2) * 1.8
      end
      if floor(code / 4) eq 0
        let b2 = 0
      else
        let b2 = (floor(code / 4) % 2) * 1.8
      end
      if floor(code / 8) eq 0
        let b3 = 0
      else
        let b3 = floor(code / 8) % 2 * 1.8
      end
      if floor(code / 16) eq 0
        let b4 = 0
      else
        let b4 = floor(code / 16) % 2 * 1.8
      end
      if floor(code / 32) eq 0
        let b5 = 0
      else
        let b5 = floor(code / 32) % 2 * 1.8
      end
      if floor(code / 64) eq 0
        let b6 = 0
      else
        let b6 = floor(code / 64) % 2 * 1.8
      end
      alter vb0 $&b0
      alter vb1 $&b1
      alter vb2 $&b2
      alter vb3 $&b3
      alter vb4 $&b4
      alter vb5 $&b5
      alter vb6 $&b6
      save v(b0) v(b1) v(b2) v(b3) v(b4) v(b5) v(b6) i(vbias) i(viout) v(vout)
      op
      wrdata ~/Documents/MADVLSI-MP4/schematic/data/dac7my_L{$&myL}W{$&myW}op-{$&run}.txt v(b0) v(b1)
+ v(b2) v(b3) v(b4) v(b5) v(b6) i(vbias) i(viout) v(vout)
      if code eq 0
        set appendwrite
        set wr_vecnames = FALSE
      end
      let code = code + 1
    end
    reset
    let run = run + 1
  end

  set appendwrite = FALSE
  reset
  set wr_singlescale
  set wr_vecnames
  alter vb0 1.8
  alter vb1 1.8
  alter vb2 1.8
  alter vb3 1.8
  alter vb4 1.8
  alter vb5 1.8
  alter vb6 1.8
  save v(b0) v(b1) v(b2) v(b3) v(b4) v(b5) v(b6) i(vbias) i(viout) v(vout)
  dc Voutt 0 1.8 0.01
  run
  wrdata ~/Documents/MADVLSI-MP4/schematic/data/dac7my_L{$&myL}W{$&myW}vout-1.txt v(b0) v(b1) v(b2) v(b3)
+ v(b4) v(b5) v(b6) i(vbias) i(viout) v(vout)

  reset
  set wr_singlescale
  set wr_vecnames
  alter vb0 1.8
  alter vb1 1.8
  alter vb2 1.8
  alter vb3 1.8
  alter vb4 1.8
  alter vb5 1.8
  alter vb6 0
  save v(b0) v(b1) v(b2) v(b3) v(b4) v(b5) v(b6) i(vbias) i(viout) v(vout)
  dc Voutt 0 1.8 0.01
  run
  wrdata ~/Documents/MADVLSI-MP4/schematic/data/dac7my_L{$&myL}W{$&myW}vout-2.txt v(b0) v(b1) v(b2) v(b3)
+ v(b4) v(b5) v(b6) i(vbias) i(viout) v(vout)

  reset
  set wr_singlescale
  set wr_vecnames
  alter vb0 1.8
  alter vb1 1.8
  alter vb2 1.8
  alter vb3 1.8
  alter vb4 1.8
  alter vb5 1.8
  alter vb6 1.8
  save v(b0) v(b1) v(b2) v(b3) v(b4) v(b5) v(b6) i(vbias) i(viout) v(vout)
  dc Vdd 0 1.8 0.01
  run
  wrdata ~/Documents/MADVLSI-MP4/schematic/data/dac7my_L{$&myL}W{$&myW}vdd-1.txt v(b0) v(b1) v(b2) v(b3)
+ v(b4) v(b5) v(b6) i(vbias) i(viout) v(vout)

  reset
  set wr_singlescale
  set wr_vecnames
  alter vb0 1.8
  alter vb1 1.8
  alter vb2 1.8
  alter vb3 1.8
  alter vb4 1.8
  alter vb5 1.8
  alter vb6 0
  save v(b0) v(b1) v(b2) v(b3) v(b4) v(b5) v(b6) i(vbias) i(viout) v(vout)
  dc Vdd 0 1.8 0.01
  run
  wrdata ~/Documents/MADVLSI-MP4/schematic/data/dac7my_L{$&myL}W{$&myW}vdd-2.txt v(b0) v(b1) v(b2) v(b3)
+ v(b4) v(b5) v(b6) i(vbias) i(viout) v(vout)
.endc
.OPTIONS ITL1=300  ITL2=100

**** end user architecture code
**.ends
.GLOBAL GND
.GLOBAL VDD
.end
